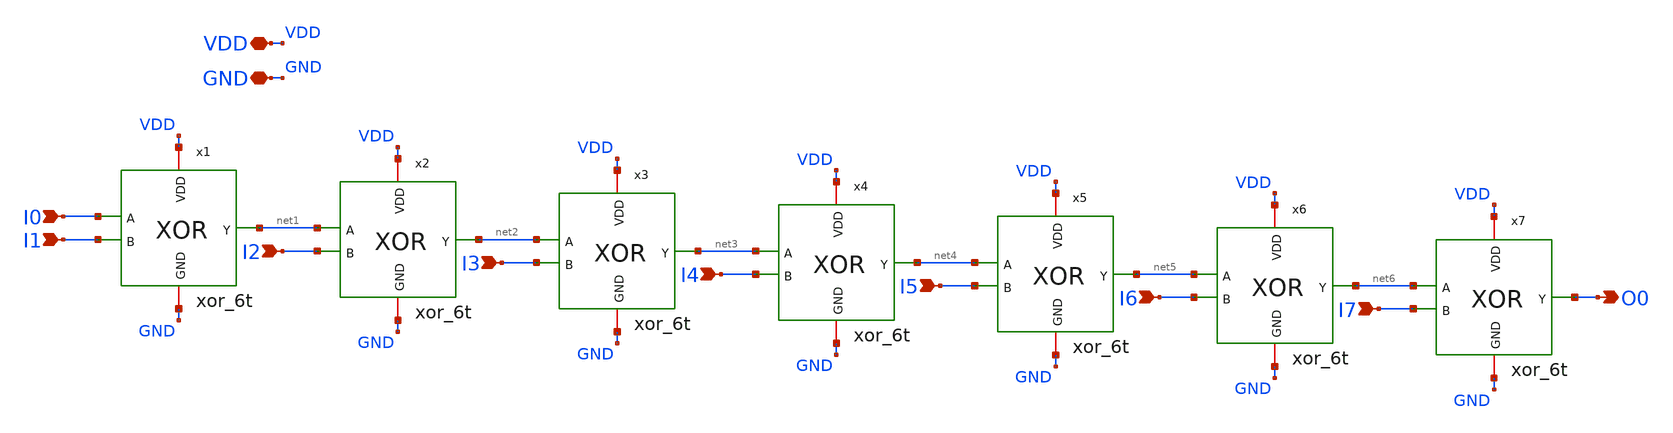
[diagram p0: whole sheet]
** sch_path: even_parity_generator/schematic/even_parity_gen_xor_6t_ub.sch
**.subckt even_parity_gen_xor_6t_ub VDD GND I0 I1 I2 I3 I4 I5 I6 I7 O0
*.iopin VDD
*.iopin GND
*.ipin I0
*.ipin I1
*.ipin I2
*.ipin I3
*.ipin I4
*.ipin I5
*.ipin I6
*.ipin I7
*.opin O0
x1 VDD net1 I0 I1 GND xor_6t
x2 VDD net2 net1 I2 GND xor_6t
x3 VDD net3 net2 I3 GND xor_6t
x4 VDD net4 net3 I4 GND xor_6t
x5 VDD net5 net4 I5 GND xor_6t
x6 VDD net6 net5 I6 GND xor_6t
x7 VDD O0 net6 I7 GND xor_6t
**.ends
.end
